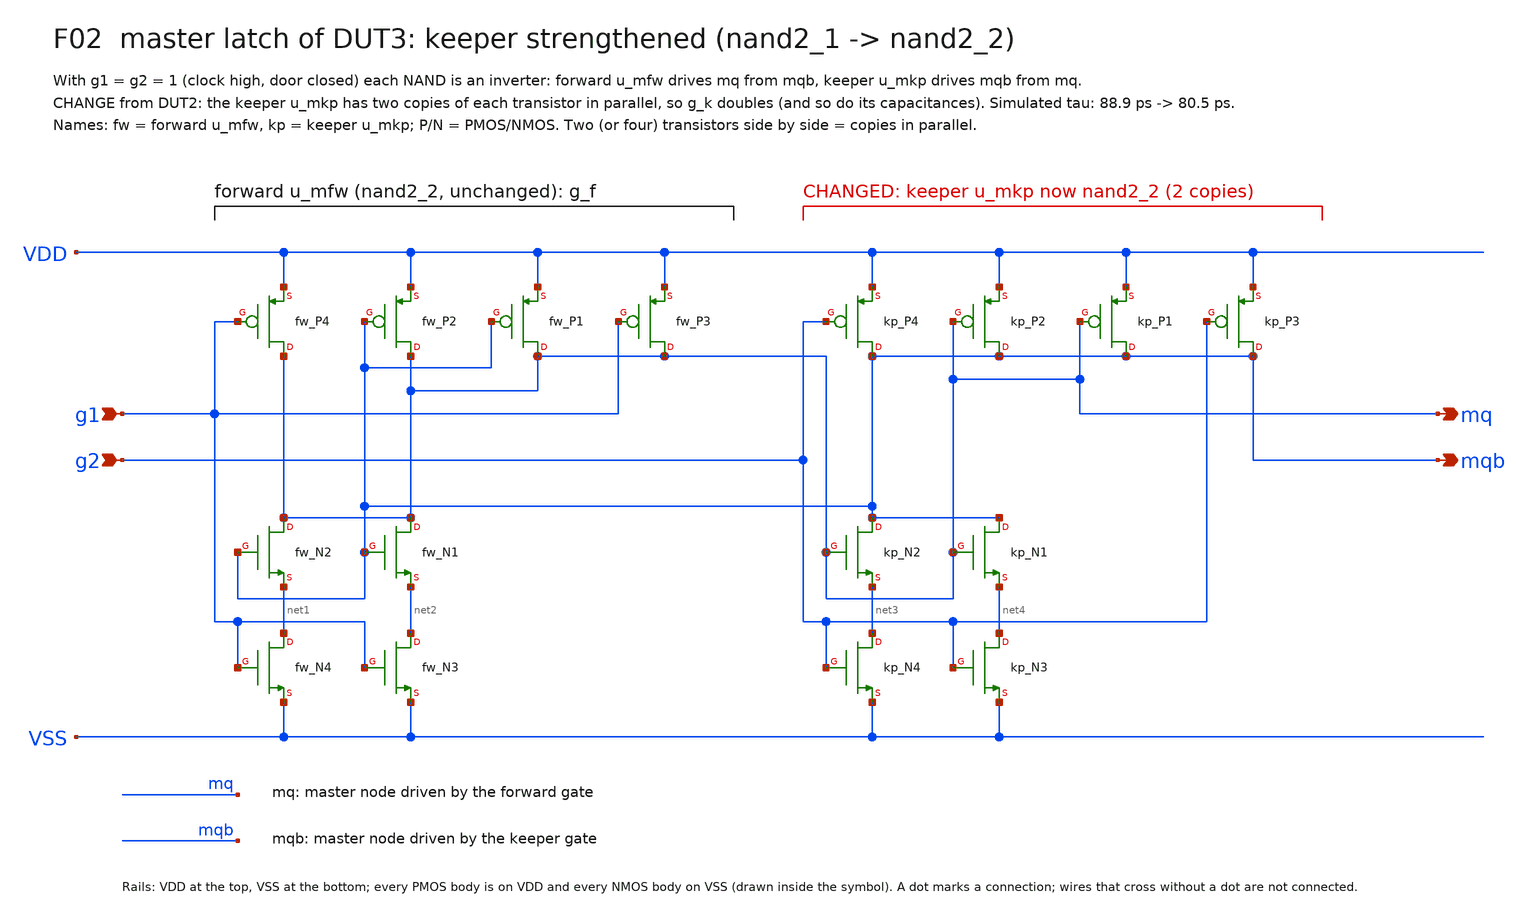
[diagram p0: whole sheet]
** sch_path: xschem/focus/F02_master_latch_keeper.sch
**.subckt F02_master_latch_keeper g1 g2 mq mqb
*.ipin g1
*.ipin g2
*.opin mq
*.opin mqb
Xfw_N4 net1 g1 VSS VSS nfet_05v0 L=0.6u W=0.82u nf=1 m=1
Xfw_N2 mq mqb net1 VSS nfet_05v0 L=0.6u W=0.82u nf=1 m=1
Xfw_N1 mq mqb net2 VSS nfet_05v0 L=0.6u W=0.82u nf=1 m=1
Xfw_N3 net2 g1 VSS VSS nfet_05v0 L=0.6u W=0.82u nf=1 m=1
Xfw_P4 mq g1 VDD VDD pfet_05v0 L=0.5u W=1.13u nf=1 m=1
Xfw_P2 mq mqb VDD VDD pfet_05v0 L=0.5u W=1.13u nf=1 m=1
Xfw_P1 mq mqb VDD VDD pfet_05v0 L=0.5u W=1.13u nf=1 m=1
Xfw_P3 mq g1 VDD VDD pfet_05v0 L=0.5u W=1.13u nf=1 m=1
Xkp_N4 net3 g2 VSS VSS nfet_05v0 L=0.6u W=0.82u nf=1 m=1
Xkp_N2 mqb mq net3 VSS nfet_05v0 L=0.6u W=0.82u nf=1 m=1
Xkp_N1 mqb mq net4 VSS nfet_05v0 L=0.6u W=0.82u nf=1 m=1
Xkp_N3 net4 g2 VSS VSS nfet_05v0 L=0.6u W=0.82u nf=1 m=1
Xkp_P4 mqb g2 VDD VDD pfet_05v0 L=0.5u W=1.13u nf=1 m=1
Xkp_P2 mqb mq VDD VDD pfet_05v0 L=0.5u W=1.13u nf=1 m=1
Xkp_P1 mqb mq VDD VDD pfet_05v0 L=0.5u W=1.13u nf=1 m=1
Xkp_P3 mqb g2 VDD VDD pfet_05v0 L=0.5u W=1.13u nf=1 m=1
**.ends
.end
